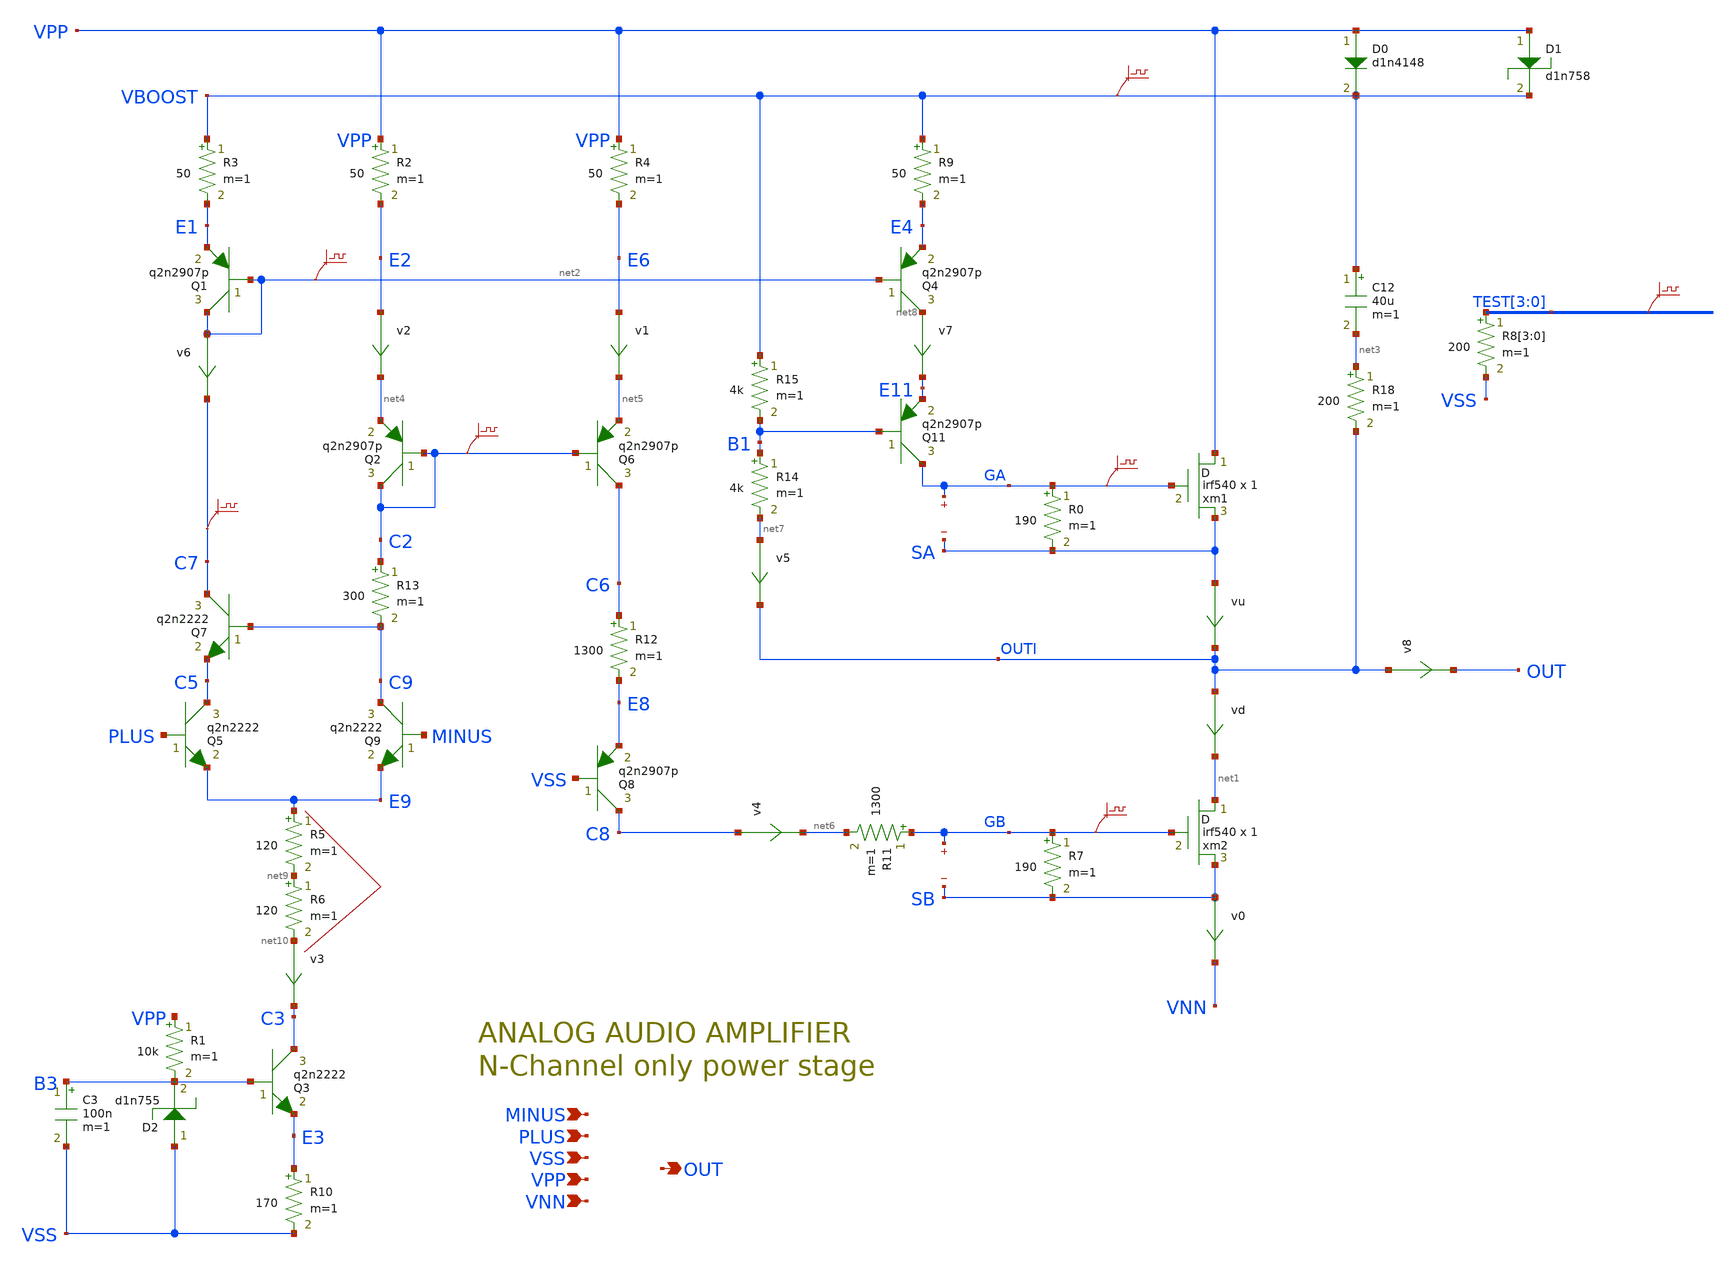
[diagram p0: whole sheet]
** sch_path: xschem_library/examples/mos_power_ampli.sch
**.subckt mos_power_ampli PLUS VPP VNN OUT MINUS VSS
*.ipin PLUS
*.ipin VPP
*.ipin VNN
*.opin OUT
*.ipin MINUS
*.ipin VSS
xm2 net1 GB SB irf540 m=1
R7 GB SB 190 m=1
xm1 VPP GA SA irf540 m=1
R0 GA SA 190 m=1
R2 VPP E2 50 m=1
R3 VBOOST E1 50 m=1
Q5 C5 PLUS E9 q2n2222 area=1 m=1
Q4 net8 net2 E4 q2n2907p area=1 m=1
R9 VBOOST E4 50 m=1
Q6 C6 C2 net5 q2n2907p area=1 m=1
R4 VPP E6 50 m=1
vd OUTI net1 0
.save i(vd)
vu SA OUTI 0
.save i(vu)
Q1 net2 net2 E1 q2n2907p area=1 m=1
Q2 C2 C2 net4 q2n2907p area=1 m=1
Q9 C9 MINUS E9 q2n2222 area=1 m=1
R11 GB net6 1300 m=1
Q8 C8 VSS E8 q2n2907p area=1 m=1
C12 VBOOST net3 40u m=1
D0 VPP VBOOST d1n4148 area=1
R18 net3 OUTI 200 m=1
D1 VPP VBOOST d1n758
R14 B1 net7 4k m=1
Q11 GA B1 E11 q2n2907p area=1 m=1
R15 VBOOST B1 4k m=1
R5 E9 net9 120 m=1
R6 net9 net10 120 m=1
D2 VSS B3 d1n755
Q3 C3 B3 E3 q2n2222 area=1 m=1
R1 VPP B3 10k m=1
R10 E3 VSS 170 m=1
C3 B3 VSS 100n m=1
R12 C6 E8 1300 m=1
R13 C2 C9 300 m=1
Q7 C7 C9 C5 q2n2222 area=1 m=1
v0 SB VNN 0
.save i(v0)
v1 E6 net5 0
.save i(v1)
v2 E2 net4 0
.save i(v2)
v3 net10 C3 0
.save i(v3)
v4 C8 net6 0
.save i(v4)
v5 net7 OUTI 0
.save i(v5)
v6 net2 C7 0
.save i(v6)
v7 net8 E11 0
.save i(v7)
.save v(gb)
.save v(sb)
.save v(ga)
.save v(sa)
v8 OUTI OUT 0
.save i(v8)
.save v(ga)
.save v(gb)
.save v(c2)
.save v(net2)
.save v(c7)
.save v(test[3])
.save v(test[2])
.save v(test[1])
.save v(test[0])
R8[3] TEST[3] VSS 200 m=1
R8[2] TEST[2] VSS 200 m=1
R8[1] TEST[1] VSS 200 m=1
R8[0] TEST[0] VSS 200 m=1
.save v(vboost)
**** begin user architecture code

.option PARHIER=LOCAL RUNLVL=6 post MODMONTE=1 warn maxwarn=6000
.option sampling_method = SRS ingold=1
.option method=gear
.option savecurrents
.temp 30



vvss vss 0 dc 0
vvpp vpp 0 dc 50
vvnn vnn 0 dc -50

rfb1 vpp minus 100k
rfb2 out minus 100k
rfb3 minus vdc '100k/43'


vvdc vdc 0 dc 21.3
eref vref 0 plus vdc 45

vplus plus vdc dc 0

evboost vboost 0 vol='v(out)>=40 ? v(out)+10 : 50'
rload out 0 4

** models are generally not free: you must download
** SPICE models for active devices and put them  into the below
** referenced file in simulation directory.
.include "models_poweramp.txt"
.dc vplus '-1.5' '1.5' 0.1
.save all
.op
*.probe dc v(plus,vdc)



* .probe v(ga,sa) v(gb,sb)
* .probe p(q*) p(r*) i(r*) p(xm1) p(xm2) i(d*)
**** end user architecture code
**.ends
.end
